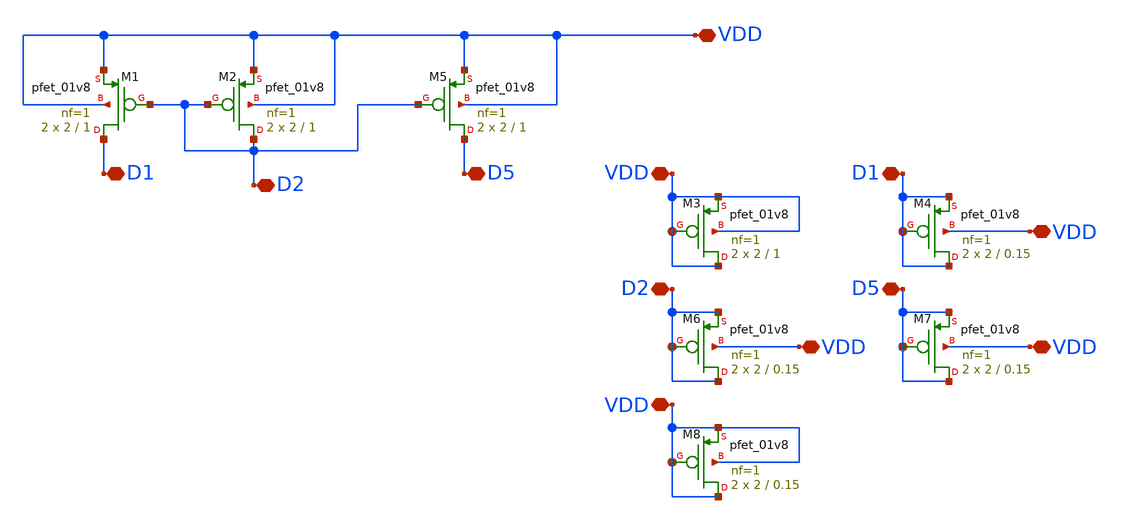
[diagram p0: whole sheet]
** sch_path: opamp/mag/pmoscs.sch
**.subckt pmoscs VDD D5 D2 D1 VDD D1 D2 D5 VDD VDD VDD VDD
*.iopin VDD
*.iopin D5
*.iopin D2
*.iopin D1
*.iopin VDD
*.iopin D1
*.iopin D2
*.iopin D5
*.iopin VDD
*.iopin VDD
*.iopin VDD
*.iopin VDD
XM1 D1 D2 VDD VDD sky130_fd_pr__pfet_01v8 L=1 W=2 nf=1 ad='int((nf+1)/2) * W/nf * 0.29' as='int((nf+2)/2) * W/nf * 0.29'
+ pd='2*int((nf+1)/2) * (W/nf + 0.29)' ps='2*int((nf+2)/2) * (W/nf + 0.29)' nrd='0.29 / W' nrs='0.29 / W'
+ sa=0 sb=0 sd=0 mult=2 m=2
XM2 D2 D2 VDD VDD sky130_fd_pr__pfet_01v8 L=1 W=2 nf=1 ad='int((nf+1)/2) * W/nf * 0.29' as='int((nf+2)/2) * W/nf * 0.29'
+ pd='2*int((nf+1)/2) * (W/nf + 0.29)' ps='2*int((nf+2)/2) * (W/nf + 0.29)' nrd='0.29 / W' nrs='0.29 / W'
+ sa=0 sb=0 sd=0 mult=2 m=2
XM5 D5 D2 VDD VDD sky130_fd_pr__pfet_01v8 L=1 W=2 nf=1 ad='int((nf+1)/2) * W/nf * 0.29' as='int((nf+2)/2) * W/nf * 0.29'
+ pd='2*int((nf+1)/2) * (W/nf + 0.29)' ps='2*int((nf+2)/2) * (W/nf + 0.29)' nrd='0.29 / W' nrs='0.29 / W'
+ sa=0 sb=0 sd=0 mult=2 m=2
XM3 VDD VDD VDD VDD sky130_fd_pr__pfet_01v8 L=1 W=2 nf=1 ad='int((nf+1)/2) * W/nf * 0.29' as='int((nf+2)/2) * W/nf * 0.29'
+ pd='2*int((nf+1)/2) * (W/nf + 0.29)' ps='2*int((nf+2)/2) * (W/nf + 0.29)' nrd='0.29 / W' nrs='0.29 / W'
+ sa=0 sb=0 sd=0 mult=2 m=2
XM4 D1 D1 D1 VDD sky130_fd_pr__pfet_01v8 L=0.15 W=2 nf=1 ad='int((nf+1)/2) * W/nf * 0.29' as='int((nf+2)/2) * W/nf * 0.29'
+ pd='2*int((nf+1)/2) * (W/nf + 0.29)' ps='2*int((nf+2)/2) * (W/nf + 0.29)' nrd='0.29 / W' nrs='0.29 / W'
+ sa=0 sb=0 sd=0 mult=2 m=2
XM6 D2 D2 D2 VDD sky130_fd_pr__pfet_01v8 L=0.15 W=2 nf=1 ad='int((nf+1)/2) * W/nf * 0.29' as='int((nf+2)/2) * W/nf * 0.29'
+ pd='2*int((nf+1)/2) * (W/nf + 0.29)' ps='2*int((nf+2)/2) * (W/nf + 0.29)' nrd='0.29 / W' nrs='0.29 / W'
+ sa=0 sb=0 sd=0 mult=2 m=2
XM7 D5 D5 D5 VDD sky130_fd_pr__pfet_01v8 L=0.15 W=2 nf=1 ad='int((nf+1)/2) * W/nf * 0.29' as='int((nf+2)/2) * W/nf * 0.29'
+ pd='2*int((nf+1)/2) * (W/nf + 0.29)' ps='2*int((nf+2)/2) * (W/nf + 0.29)' nrd='0.29 / W' nrs='0.29 / W'
+ sa=0 sb=0 sd=0 mult=2 m=2
XM8 VDD VDD VDD VDD sky130_fd_pr__pfet_01v8 L=0.15 W=2 nf=1 ad='int((nf+1)/2) * W/nf * 0.29' as='int((nf+2)/2) * W/nf * 0.29'
+ pd='2*int((nf+1)/2) * (W/nf + 0.29)' ps='2*int((nf+2)/2) * (W/nf + 0.29)' nrd='0.29 / W' nrs='0.29 / W'
+ sa=0 sb=0 sd=0 mult=2 m=2
**.ends
.end
